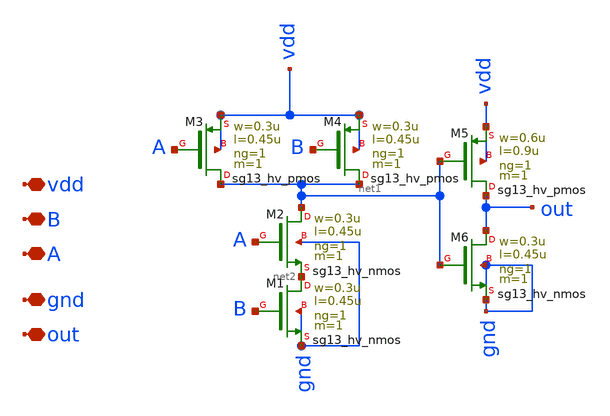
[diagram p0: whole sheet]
** sch_path: dependencies/OTA/OTA-main/schematic/xschem/Clock_gen_using_transistor_hv/and.sch
**.subckt and vdd B A gnd out
*.iopin vdd
*.iopin B
*.iopin A
*.iopin gnd
*.iopin out
XM3 net1 A vdd vdd sg13_hv_pmos w=0.3u l=0.45u ng=1 m=1 mm_ok=1
XM1 net2 B gnd gnd sg13_hv_nmos w=0.3u l=0.45u ng=1 m=1 mm_ok=1
XM2 net1 A net2 gnd sg13_hv_nmos w=0.3u l=0.45u ng=1 m=1 mm_ok=1
XM4 net1 B vdd vdd sg13_hv_pmos w=0.3u l=0.45u ng=1 m=1 mm_ok=1
XM5 out net1 vdd vdd sg13_hv_pmos w=0.6u l=0.9u ng=1 m=1 mm_ok=1
XM6 out net1 gnd gnd sg13_hv_nmos w=0.3u l=0.45u ng=1 m=1 mm_ok=1
**.ends
.end
